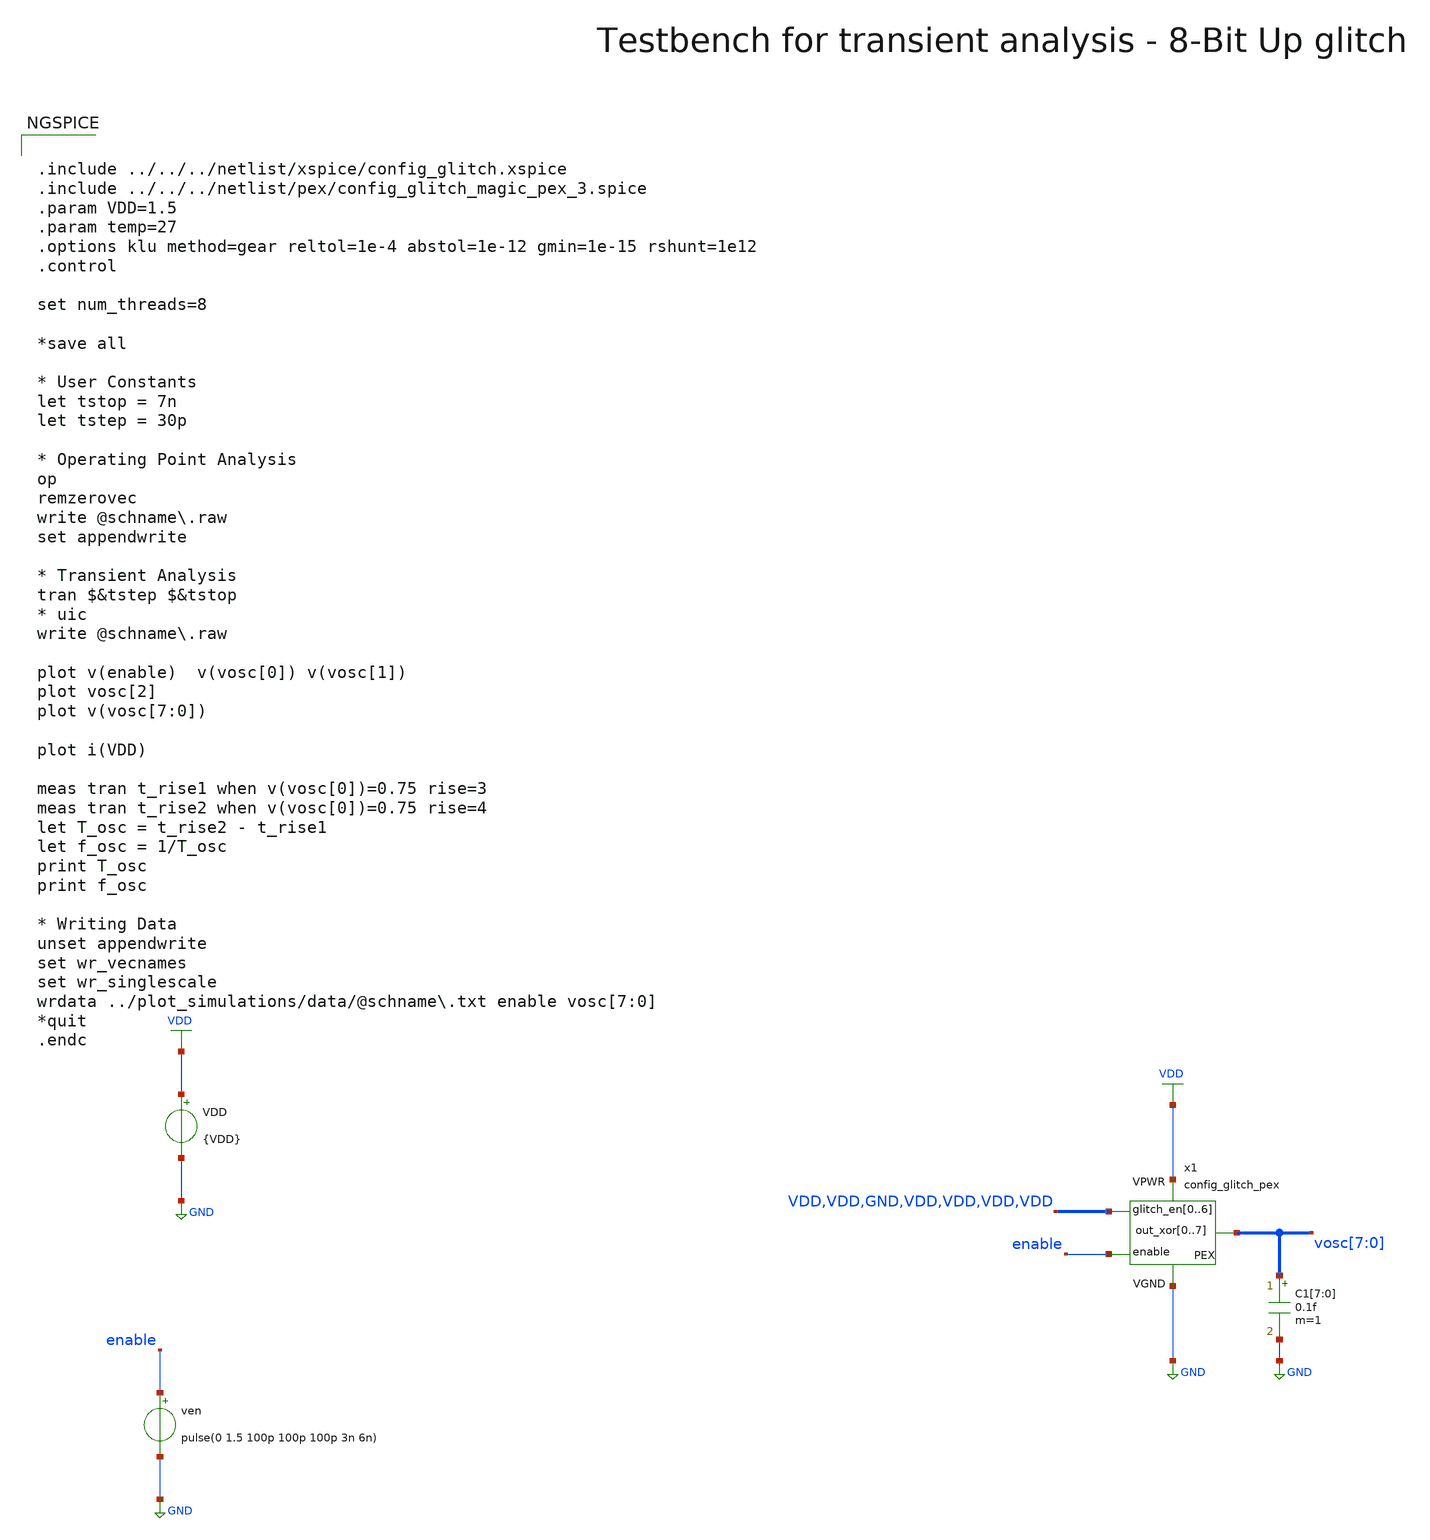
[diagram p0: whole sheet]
** sch_path: macros/heichips26_digital_project/macros/config_glitch/testbenches/xschem/config_glitch_tb_tran.sch
**.subckt config_glitch_tb_tran
VDD VDD GND {VDD}
ven enable GND pulse(0 1.5 100p 100p 100p 3n 6n)
C1[7] vosc[7] GND 0.1f m=1
C1[6] vosc[6] GND 0.1f m=1
C1[5] vosc[5] GND 0.1f m=1
C1[4] vosc[4] GND 0.1f m=1
C1[3] vosc[3] GND 0.1f m=1
C1[2] vosc[2] GND 0.1f m=1
C1[1] vosc[1] GND 0.1f m=1
C1[0] vosc[0] GND 0.1f m=1
x1 VDD GND enable vosc[7] vosc[6] vosc[5] vosc[4] vosc[3] vosc[2] vosc[1] vosc[0] VDD VDD GND VDD
+ VDD VDD VDD config_glitch_pex
**** begin user architecture code


.include ../../../netlist/xspice/config_glitch.xspice
.include ../../../netlist/pex/config_glitch_magic_pex_3.spice
.param VDD=1.5
.param temp=27
.options klu method=gear reltol=1e-4 abstol=1e-12 gmin=1e-15 rshunt=1e12
.control

set num_threads=8

*save all

* User Constants
let tstop = 7n
let tstep = 30p

* Operating Point Analysis
op
remzerovec
write @schname\.raw
set appendwrite

* Transient Analysis
tran $&tstep $&tstop
* uic
write @schname\.raw

plot v(enable)  v(vosc[0]) v(vosc[1])
plot vosc[2]
plot v(vosc[7:0])

plot i(VDD)

meas tran t_rise1 when v(vosc[0])=0.75 rise=3
meas tran t_rise2 when v(vosc[0])=0.75 rise=4
let T_osc = t_rise2 - t_rise1
let f_osc = 1/T_osc
print T_osc
print f_osc

* Writing Data
unset appendwrite
set wr_vecnames
set wr_singlescale
wrdata ../plot_simulations/data/@schname\.txt enable vosc[7:0]
*quit
.endc


.lib cornerMOSlv.lib mos_tt
.lib cornerMOShv.lib mos_tt
.lib cornerRES.lib res_typ
.lib cornerDIO.lib dio_tt

**** end user architecture code
**.ends
.GLOBAL GND
.GLOBAL VDD
.end
